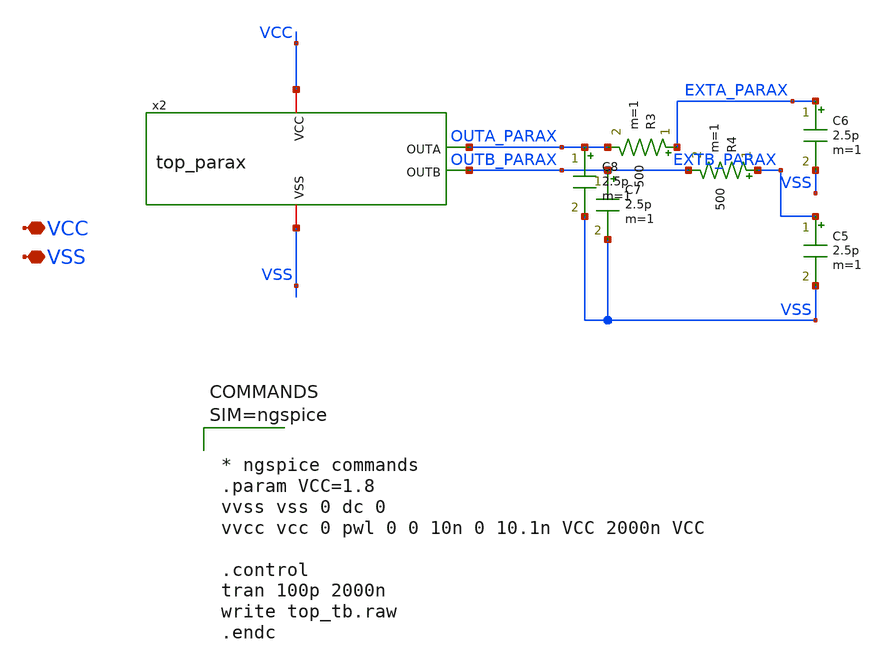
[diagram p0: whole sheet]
** sch_path: xschem/top_tb_postL.sch
**.subckt top_tb_postL VCC VSS
*.iopin VCC
*.iopin VSS
x2 VCC OUTA_PARAX OUTB_PARAX VSS top_parax
R3 EXTA_PARAX OUTA_PARAX 500 m=1
R4 EXTB_PARAX OUTB_PARAX 500 m=1
C5 EXTB_PARAX VSS 2.5p m=1
C6 EXTA_PARAX VSS 2.5p m=1
C7 OUTB_PARAX VSS 2.5p m=1
C8 OUTA_PARAX VSS 2.5p m=1
**** begin user architecture code

** opencircuitdesign pdks install
.lib $::SKYWATER_MODELS/sky130.lib.spice tt





* ngspice commands
.param VCC=1.8
vvss vss 0 dc 0
vvcc vcc 0 pwl 0 0 10n 0 10.1n VCC 2000n VCC

.control
tran 100p 2000n
write top_tb.raw
.endc




**** end user architecture code
**.ends

* expanding   symbol:  top_parax.sym # of pins=4
** sym_path: xschem/top.sym
.include [file normalize ../mag/top.sim.spice]
.end
